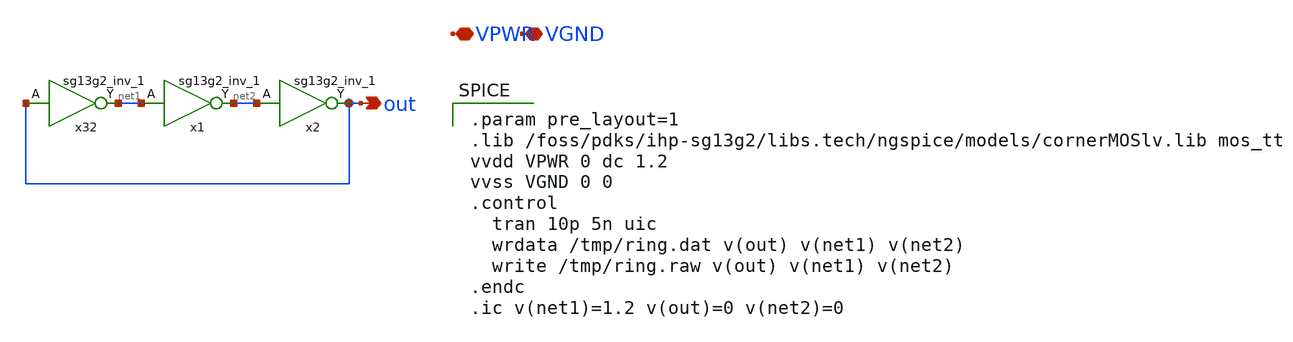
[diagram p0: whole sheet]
** sch_path: analog/inverter_ring_oscillator/schematic/main.sch
**.subckt main out VPWR VGND
*.opin out
*.iopin VPWR
*.iopin VGND
x32 net1 out VPWR VGND sg13g2_inv_1
x1 net2 net1 VPWR VGND sg13g2_inv_1
x2 out net2 VPWR VGND sg13g2_inv_1
**** begin user architecture code

.param pre_layout=1
.lib /foss/pdks/ihp-sg13g2/libs.tech/ngspice/models/cornerMOSlv.lib mos_tt
vvdd VPWR 0 dc 1.2
vvss VGND 0 0
.control
  tran 10p 5n uic
  wrdata /tmp/ring.dat v(out) v(net1) v(net2)
  write /tmp/ring.raw v(out) v(net1) v(net2)
.endc
.ic v(net1)=1.2 v(out)=0 v(net2)=0


**** end user architecture code
**.ends

* expanding   symbol:  sg13g2_inv_1.sym # of pins=2
** sym_path: sg13g2_inv_1.sym
** sch_path: sg13g2_inv_1.sch
.subckt sg13g2_inv_1 Y A VDD VSS
*.opin Y
*.ipin A
*.iopin VDD
*.iopin VSS
XM1 Y A VSS VSS sg13_lv_nmos w=740.00n l=130.00n ng=1 m=1 mm_ok=1
XM2 Y A VDD VDD sg13_lv_pmos w=1.12u l=130.00n ng=1 m=1 mm_ok=1
.ends

.end
